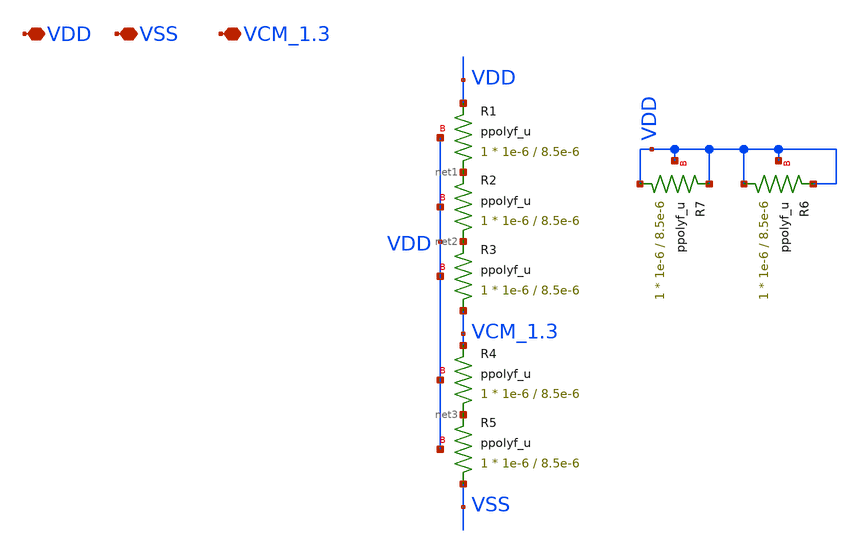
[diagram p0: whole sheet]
** sch_path: AWG_OUTPUT_AND_MUX_PAKISTAN_05/xschem/RES_VCM_1.3.sch
**.subckt RES_VCM_1.3 VDD VSS VCM_1.3
*.iopin VDD
*.iopin VSS
*.iopin VCM_1.3
XR1 net1 VDD VDD ppolyf_u r_width=1e-6 r_length=8.5e-6 m=1
XR2 net2 net1 VDD ppolyf_u r_width=1e-6 r_length=8.5e-6 m=1
XR3 VCM_1.3 net2 VDD ppolyf_u r_width=1e-6 r_length=8.5e-6 m=1
XR4 net3 VCM_1.3 VDD ppolyf_u r_width=1e-6 r_length=8.5e-6 m=1
XR5 VSS net3 VDD ppolyf_u r_width=1e-6 r_length=8.5e-6 m=1
XR6 VDD VDD VDD ppolyf_u r_width=1e-6 r_length=8.5e-6 m=1
XR7 VDD VDD VDD ppolyf_u r_width=1e-6 r_length=8.5e-6 m=1
**.ends
.end
